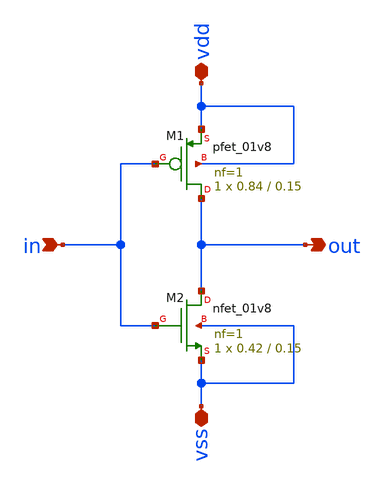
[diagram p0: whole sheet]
** sch_path: sch/PLL_caravel/NOT.sch
**.subckt NOT vdd vss in out
*.iopin vdd
*.iopin vss
*.ipin in
*.opin out
XM1 out in vdd vdd sky130_fd_pr__pfet_01v8 L=0.15 W=0.84 nf=1 ad='int((nf+1)/2) * W/nf * 0.29' as='int((nf+2)/2) * W/nf * 0.29'
+ pd='2*int((nf+1)/2) * (W/nf + 0.29)' ps='2*int((nf+2)/2) * (W/nf + 0.29)' nrd='0.29 / W' nrs='0.29 / W'
+ sa=0 sb=0 sd=0 mult=1 m=1
XM2 out in vss vss sky130_fd_pr__nfet_01v8 L=0.15 W=0.42 nf=1 ad='int((nf+1)/2) * W/nf * 0.29' as='int((nf+2)/2) * W/nf * 0.29'
+ pd='2*int((nf+1)/2) * (W/nf + 0.29)' ps='2*int((nf+2)/2) * (W/nf + 0.29)' nrd='0.29 / W' nrs='0.29 / W'
+ sa=0 sb=0 sd=0 mult=1 m=1
**.ends
.end
